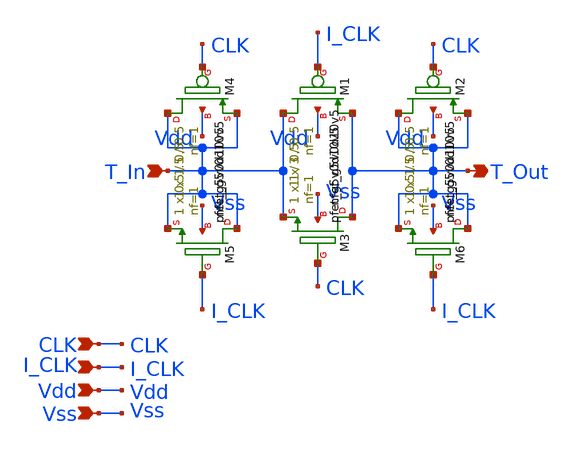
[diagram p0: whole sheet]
** sch_path: xschem/T-gate.sch
**.subckt T-gate T_In T_Out Vdd Vss I_CLK CLK
*.ipin T_In
*.opin T_Out
*.ipin Vdd
*.ipin Vss
*.ipin I_CLK
*.ipin CLK
XM1 T_In I_CLK T_Out Vdd sky130_fd_pr__pfet_g5v0d10v5 L=0.5 W=3 nf=1 ad='int((1 + 1)/2) * 3 / 1 * 0.29'
+ as='int((1 + 2)/2) * 3 / 1 * 0.29' pd='2*int((1 + 1)/2) * (3 / 1 + 0.29)' ps='2*int((1 + 2)/2) * (3 / 1 + 0.29)'
+ nrd='0.29 / 3 ' nrs='0.29 / 3 ' sa=0 sb=0 sd=0 mult=1 m=1
XM3 T_Out CLK T_In Vss sky130_fd_pr__nfet_g5v0d10v5 L=0.5 W=1 nf=1 ad='int((1 + 1)/2) * 1 / 1 * 0.29'
+ as='int((1 + 2)/2) * 1 / 1 * 0.29' pd='2*int((1 + 1)/2) * (1 / 1 + 0.29)' ps='2*int((1 + 2)/2) * (1 / 1 + 0.29)'
+ nrd='0.29 / 1 ' nrs='0.29 / 1 ' sa=0 sb=0 sd=0 mult=1 m=1
XM2 T_Out CLK T_Out Vdd sky130_fd_pr__pfet_g5v0d10v5 L=0.5 W=1.5 nf=1 ad='int((1 + 1)/2) * 1.5 / 1 * 0.29'
+ as='int((1 + 2)/2) * 1.5 / 1 * 0.29' pd='2*int((1 + 1)/2) * (1.5 / 1 + 0.29)' ps='2*int((1 + 2)/2) * (1.5 / 1 + 0.29)'
+ nrd='0.29 / 1.5 ' nrs='0.29 / 1.5 ' sa=0 sb=0 sd=0 mult=1 m=1
XM4 T_In CLK T_In Vdd sky130_fd_pr__pfet_g5v0d10v5 L=0.5 W=1.5 nf=1 ad='int((1 + 1)/2) * 1.5 / 1 * 0.29'
+ as='int((1 + 2)/2) * 1.5 / 1 * 0.29' pd='2*int((1 + 1)/2) * (1.5 / 1 + 0.29)' ps='2*int((1 + 2)/2) * (1.5 / 1 + 0.29)'
+ nrd='0.29 / 1.5 ' nrs='0.29 / 1.5 ' sa=0 sb=0 sd=0 mult=1 m=1
XM5 T_In I_CLK T_In Vss sky130_fd_pr__nfet_g5v0d10v5 L=0.5 W=0.5 nf=1 ad='int((1 + 1)/2) * 0.5 / 1 * 0.29'
+ as='int((1 + 2)/2) * 0.5 / 1 * 0.29' pd='2*int((1 + 1)/2) * (0.5 / 1 + 0.29)' ps='2*int((1 + 2)/2) * (0.5 / 1 + 0.29)'
+ nrd='0.29 / 0.5 ' nrs='0.29 / 0.5 ' sa=0 sb=0 sd=0 mult=1 m=1
XM6 T_Out I_CLK T_Out Vss sky130_fd_pr__nfet_g5v0d10v5 L=0.5 W=0.5 nf=1 ad='int((1 + 1)/2) * 0.5 / 1 * 0.29'
+ as='int((1 + 2)/2) * 0.5 / 1 * 0.29' pd='2*int((1 + 1)/2) * (0.5 / 1 + 0.29)' ps='2*int((1 + 2)/2) * (0.5 / 1 + 0.29)'
+ nrd='0.29 / 0.5 ' nrs='0.29 / 0.5 ' sa=0 sb=0 sd=0 mult=1 m=1
**.ends
.end
